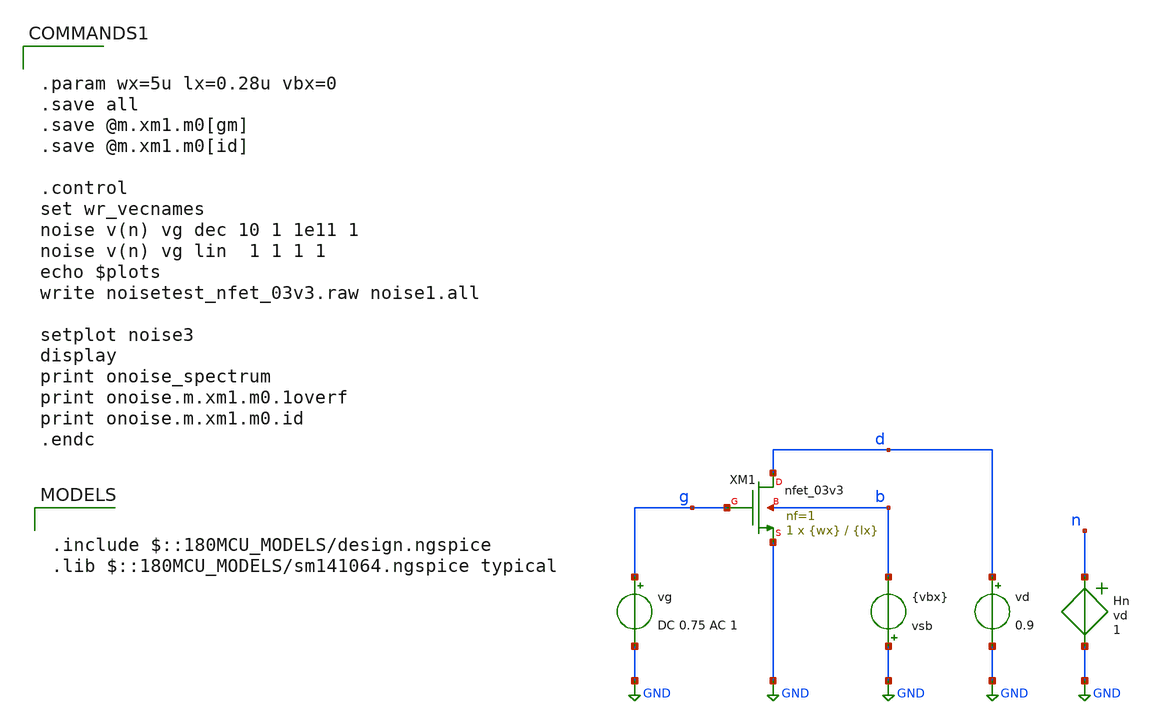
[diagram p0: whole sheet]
** sch_path: designs/libs/bmurmann_gmoverid/gf180mcuD/noisetest_nfet_03v3.sch
**.subckt noisetest_nfet_03v3
vg g GND DC 0.75 AC 1
vd d GND 0.9
vsb GND b {vbx}
Hn n GND vd 1
XM1 d g GND b nfet_03v3 L={lx} W={wx} nf=1 ad='int((nf+1)/2) * W/nf * 0.18u' as='int((nf+2)/2) * W/nf * 0.18u'
+ pd='2*int((nf+1)/2) * (W/nf + 0.18u)' ps='2*int((nf+2)/2) * (W/nf + 0.18u)' nrd='0.18u / W' nrs='0.18u / W'
+ sa=0 sb=0 sd=0 m=1
**** begin user architecture code


.param wx=5u lx=0.28u vbx=0
.save all
.save @m.xm1.m0[gm]
.save @m.xm1.m0[id]

.control
set wr_vecnames
noise v(n) vg dec 10 1 1e11 1
noise v(n) vg lin  1 1 1 1
echo $plots
write noisetest_nfet_03v3.raw noise1.all

setplot noise3
display
print onoise_spectrum
print onoise.m.xm1.m0.1overf
print onoise.m.xm1.m0.id
.endc



.include $::180MCU_MODELS/design.ngspice
.lib $::180MCU_MODELS/sm141064.ngspice typical

**** end user architecture code
**.ends
.GLOBAL GND
.end
